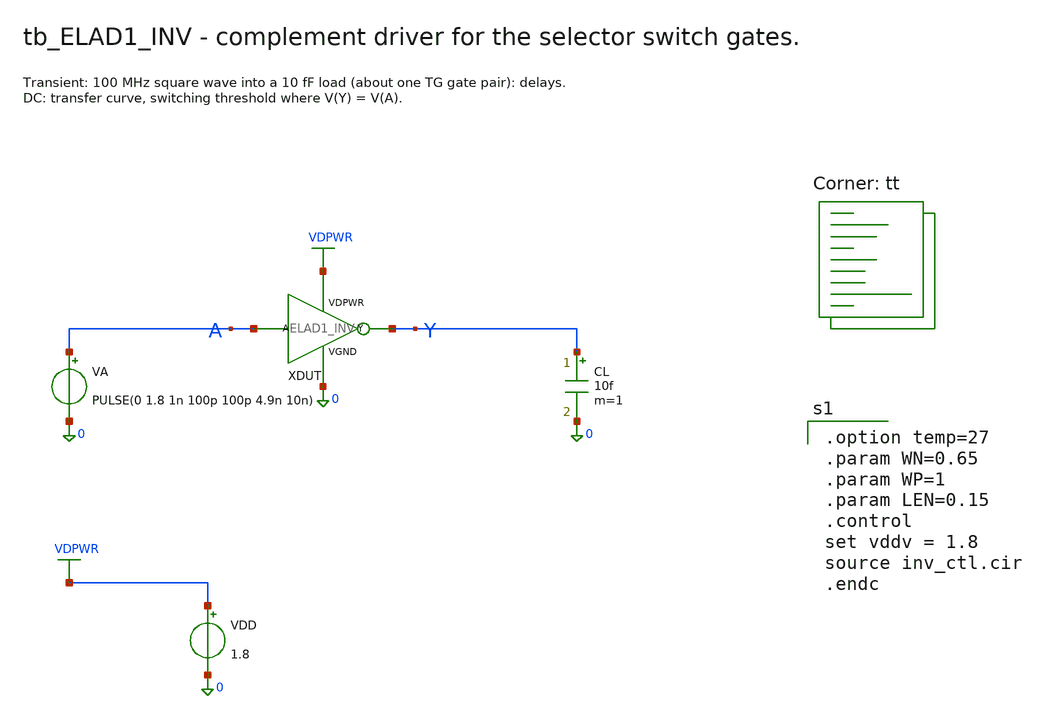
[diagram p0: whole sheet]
** sch_path: cells/ELAD1_INV/schematic/tb_ELAD1_INV.sch
**.subckt tb_ELAD1_INV
XDUT A Y VDPWR 0 ELAD1_INV
VA A 0 PULSE(0 1.8 1n 100p 100p 4.9n 10n)
CL Y 0 10f m=1
VDD VDPWR 0 1.8
**** begin user architecture code

.option temp=27
.param WN=0.65
.param WP=1
.param LEN=0.15
.control
set vddv = 1.8
source inv_ctl.cir
.endc

.lib $::SKYWATER_MODELS/sky130.lib.spice tt
**** end user architecture code
**.ends

* expanding   symbol:  ELAD1_INV.sym # of pins=4
** sym_path: cells/ELAD1_INV/schematic/ELAD1_INV.sym
** sch_path: cells/ELAD1_INV/schematic/ELAD1_INV.sch
.subckt ELAD1_INV A Y VDPWR VGND
*.iopin A
*.iopin Y
*.iopin VDPWR
*.iopin VGND
XMP Y A VDPWR VDPWR sky130_fd_pr__pfet_01v8 L=0.15 W=1 nf=1 ad='int((nf+1)/2) * W/nf * 0.29' as='int((nf+2)/2) * W/nf * 0.29'
+ pd='2*int((nf+1)/2) * (W/nf + 0.29)' ps='2*int((nf+2)/2) * (W/nf + 0.29)' nrd='0.29 / W' nrs='0.29 / W'
+ sa=0 sb=0 sd=0 mult=1 m=1
XMN Y A VGND VGND sky130_fd_pr__nfet_01v8 L=0.15 W=0.65 nf=1 ad='int((1 + 1)/2) * 0.65 / 1 * 0.29' as='int((1 + 2)/2) * 0.65 / 1 * 0.29'
+ pd='2*int((1 + 1)/2) * (0.65 / 1 + 0.29)' ps='2*int((1 + 2)/2) * (0.65 / 1 + 0.29)' nrd='0.29 / 0.65 '
+ nrs='0.29 / 0.65 ' sa=0 sb=0 sd=0 mult=1 m=1
.ends

.end
